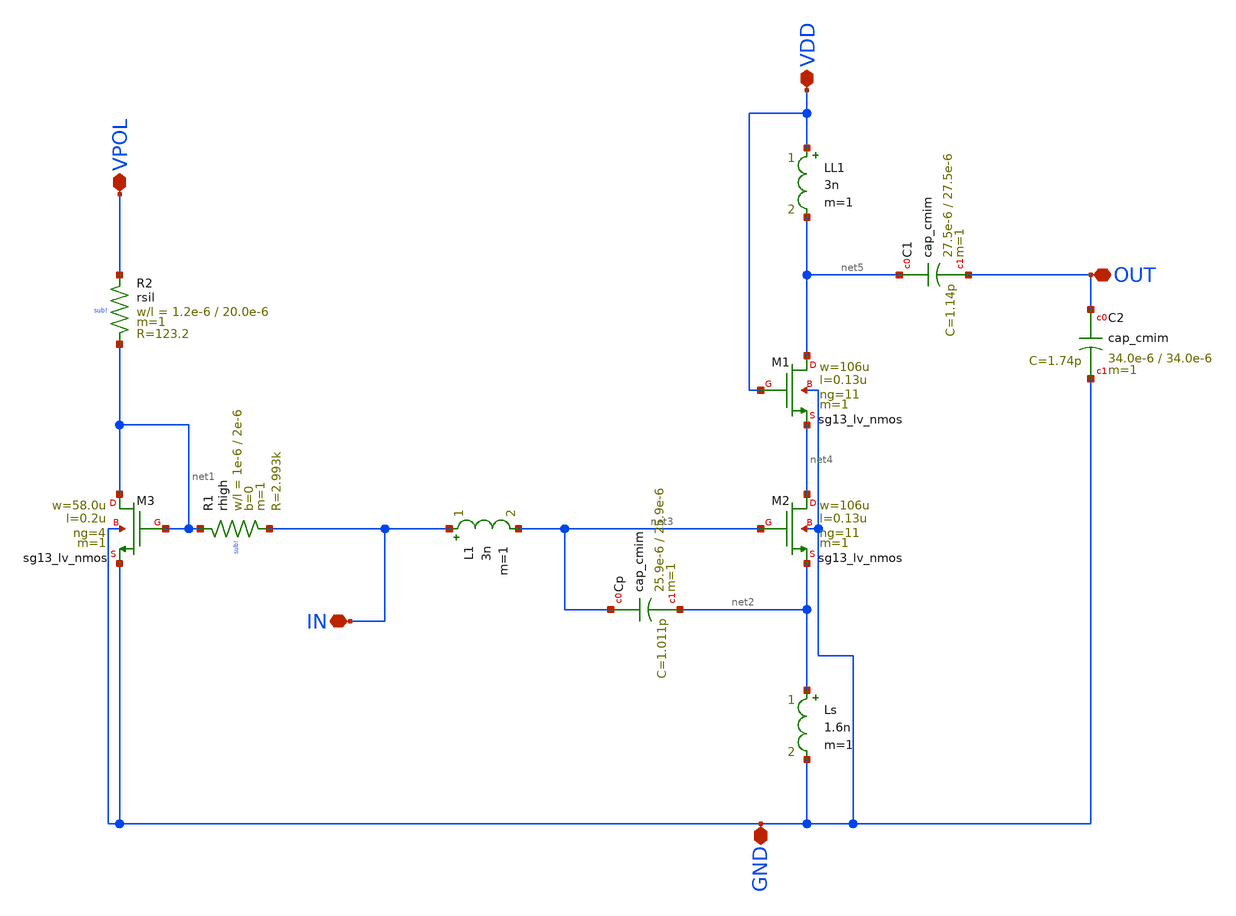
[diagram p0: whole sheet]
** sch_path: LNA_Ind_degen/LNA_prj/LNA_xschem.sch
**.subckt LNA_xschem OUT IN GND VDD VPOL
*.iopin OUT
*.iopin IN
*.iopin GND
*.iopin VDD
*.iopin VPOL
XC1 net5 OUT cap_cmim w=27.5e-6 l=27.5e-6 m=1 mm_ok=1
XM1 net5 VDD net4 GND sg13_lv_nmos w=106u l=0.13u ng=11 m=1 mm_ok=1
XR1 net1 IN sub! rhigh w=1e-6 l=2e-6 m=1 b=0 mm_ok=1
XR2 VPOL net1 sub! rsil w=1.2e-6 l=20.0e-6 m=1 mm_ok=1
XM2 net4 net3 net2 GND sg13_lv_nmos w=106u l=0.13u ng=11 m=1 mm_ok=1
XM3 net1 net1 GND GND sg13_lv_nmos w=58.0u l=0.2u ng=4 m=1 mm_ok=1
XC2 OUT GND cap_cmim w=34.0e-6 l=34.0e-6 m=1 mm_ok=1
XCp net3 net2 cap_cmim w=25.9e-6 l=25.9e-6 m=1 mm_ok=1
Ls net2 GND 1.6n m=1
LL1 VDD net5 3n m=1
L1 IN net3 3n m=1
**.ends
.end
